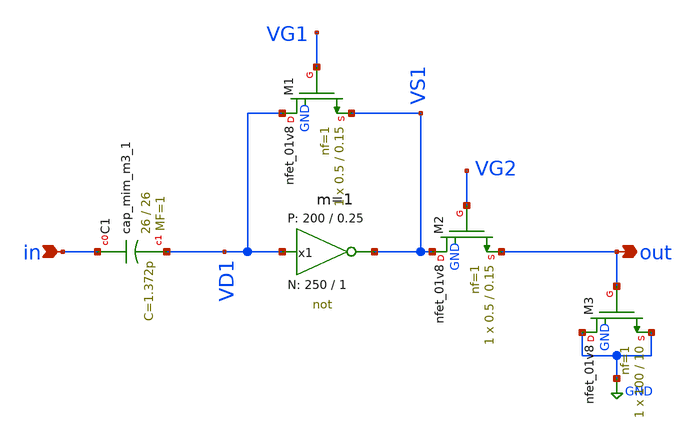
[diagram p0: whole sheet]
** sch_path: Amplifier_Inv/xschem/v4/inv_sky130_a_v4.sch
* StefanSchippers/xschem_sky130/sky130_tests/not.sch:
* Copyright 2021 Stefan Frederik Schippers
* Licensed under the Apache License, Version 2.0 (the "License");
**.subckt inv_sky130_a_v4 in out
*.ipin in
*.opin out
x1 VS1 VD1 VCC VSS not W_N=250 L_N=1 W_P=200 L_P=0.25 m=1
XC1 in VD1 sky130_fd_pr__cap_mim_m3_1 W=26 L=26 MF=1 m=1
XM1 VD1 VG1 VS1 GND sky130_fd_pr__nfet_01v8 L=0.15 W=0.5 nf=1 ad='int((nf+1)/2) * W/nf * 0.29' as='int((nf+2)/2) * W/nf * 0.29'
+ pd='2*int((nf+1)/2) * (W/nf + 0.29)' ps='2*int((nf+2)/2) * (W/nf + 0.29)' nrd='0.29 / W' nrs='0.29 / W'
+ sa=0 sb=0 sd=0 mult=1 m=1
XM2 VS1 VG2 out GND sky130_fd_pr__nfet_01v8 L=0.15 W=0.5 nf=1 ad='int((nf+1)/2) * W/nf * 0.29' as='int((nf+2)/2) * W/nf * 0.29'
+ pd='2*int((nf+1)/2) * (W/nf + 0.29)' ps='2*int((nf+2)/2) * (W/nf + 0.29)' nrd='0.29 / W' nrs='0.29 / W'
+ sa=0 sb=0 sd=0 mult=1 m=1
XM3 GND out GND GND sky130_fd_pr__nfet_01v8 L=10 W=100 nf=1 ad='int((nf+1)/2) * W/nf * 0.29' as='int((nf+2)/2) * W/nf * 0.29'
+ pd='2*int((nf+1)/2) * (W/nf + 0.29)' ps='2*int((nf+2)/2) * (W/nf + 0.29)' nrd='0.29 / W' nrs='0.29 / W'
+ sa=0 sb=0 sd=0 mult=1 m=1
**.ends

* expanding   symbol:  sky130_tests/not.sym # of pins=2
** sym_path: sky130_tests/not.sym
** sch_path: sky130_tests/not.sch
.subckt not y a VCCPIN VSSPIN     W_N=1 L_N=0.15 W_P=2 L_P=0.15
*.opin y
*.ipin a
XM1 DN a VSSPIN VSSPIN sky130_fd_pr__nfet_01v8 L=L_N W=W_N nf=1 ad='int((1 + 1)/2) * W_N / 1 * 0.29'
+ as='int((1 + 2)/2) * W_N / 1 * 0.29' pd='2*int((1 + 1)/2) * (W_N / 1 + 0.29)' ps='2*int((1 + 2)/2) * (W_N / 1 + 0.29)'
+ nrd='0.29 / W_N ' nrs='0.29 / W_N ' sa=0 sb=0 sd=0 mult=1 m=1
XM2 DP a VCCPIN VCCPIN sky130_fd_pr__pfet_01v8 L=L_P W=W_P nf=1 ad='int((nf+1)/2) * W/nf * 0.29' as='int((nf+2)/2) * W/nf * 0.29'
+ pd='2*int((nf+1)/2) * (W/nf + 0.29)' ps='2*int((nf+2)/2) * (W/nf + 0.29)' nrd='0.29 / W' nrs='0.29 / W'
+ sa=0 sb=0 sd=0 mult=1 m=1
Vmeas DP y 0
.save i(vmeas)
Vmeas1 y DN 0
.save i(vmeas1)
.save v(dp)
.save v(dn)
.ends

.GLOBAL GND
.end
